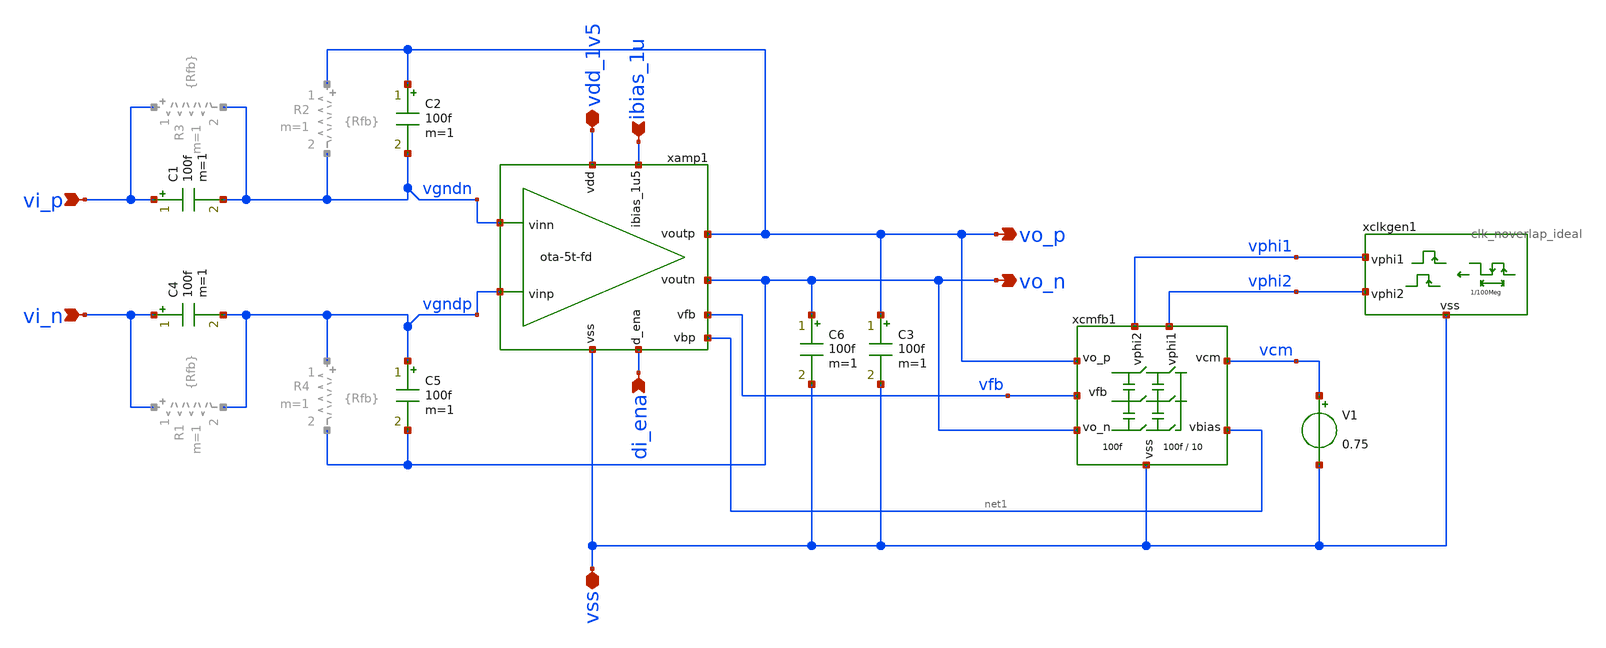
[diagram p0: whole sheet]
** sch_path: xschem/amp-cfb.sch
* xschem/ota-5t-fd.sch:
* (c) 2025 M. Koefinger
**.subckt amp-cfb vi_p vi_n di_ena vss vdd_1v5 ibias_1u vo_n vo_p
*.ipin vi_p
*.ipin vi_n
*.ipin di_ena
*.iopin vss
*.iopin vdd_1v5
*.ipin ibias_1u
*.opin vo_n
*.opin vo_p
C1 vi_p vgndn 100f m=1
C2 vo_p vgndn 100f m=1
C3 vo_p vss 100f m=1
C4 vi_n vgndp 100f m=1
C5 vgndp vo_n 100f m=1
C6 vo_n vss 100f m=1
xamp1 vdd_1v5 vfb vo_p vo_n vgndp vgndn ibias_1u di_ena vss net1 ota-5t-fd
xcmfb1 vphi1 vphi2 vss vo_p vcm net1 vfb vo_n cmfb_sc cap=100f div=10
xclkgen1 vphi1 vphi2 vss clk_noverlap_ideal fs=100Meg tnover=2n tdelay=0 trf=0.1n
V1 vcm vss 0.75
**.ends

* expanding   symbol:  ota-5t-fd.sym # of pins=10
** sym_path: xschem/ota-5t-fd.sym
** sch_path: xschem/ota-5t-fd.sch
.subckt ota-5t-fd vdd vfb voutp voutn vinp vinn ibias_1u5 d_ena vss vbp
*.ipin ibias_1u5
*.iopin vdd
*.iopin vss
*.ipin vinp
*.ipin vinn
*.opin voutn
*.ipin d_ena
*.opin voutp
*.ipin vfb
*.opin vbp
XMN3 tail gate_n vss vss sg13_lv_nmos w=2.5u l=0.5u ng=5 m=1 mm_ok=1
XMP2 voutp vfb vdd vdd sg13_lv_pmos w=0.5u l=0.5u ng=1 m=1 mm_ok=1
XMN1 voutn vinp tail vss sg13_lv_nmos w=5.5u l=0.5u ng=11 m=1 mm_ok=1
XMN2 voutp vinn tail vss sg13_lv_nmos w=5.5u l=0.5u ng=11 m=1 mm_ok=1
XMP1 voutn vfb vdd vdd sg13_lv_pmos w=0.5u l=0.5u ng=1 m=1 mm_ok=1
XMN4 ibias_1u5 gate_n vss vss sg13_lv_nmos w=1.5u l=0.5u ng=3 m=1 mm_ok=1
XMN5 gate_n ena_n vss vss sg13_lv_nmos w=0.5u l=0.13u ng=1 m=1 mm_ok=1
XMPSW1 vfb ena vdd vdd sg13_lv_pmos w=1.5u l=0.13u ng=1 m=1 mm_ok=1
XMN8 ena ena_n vss vss sg13_lv_nmos w=0.5u l=0.13u ng=1 m=1 mm_ok=1
XMP5 ena ena_n vdd vdd sg13_lv_pmos w=1.5u l=0.13u ng=1 m=1 mm_ok=1
XMN6 ibias_1u5 ena gate_n vss sg13_lv_nmos w=0.5u l=0.13u ng=1 m=1 mm_ok=1
XMN7 ena_n d_ena vss vss sg13_lv_nmos w=0.5u l=0.13u ng=1 m=1 mm_ok=1
XMP4 ena_n d_ena vdd vdd sg13_lv_pmos w=1.5u l=0.13u ng=1 m=1 mm_ok=1
XMN9 vbp gate_n vss vss sg13_lv_nmos w=1u l=0.5u ng=2 m=1 mm_ok=1
XMP3 vbp vbp vdd vdd sg13_lv_pmos w=0.5u l=0.5u ng=1 m=1 mm_ok=1
.ends


* expanding   symbol:  cmfb_sc.sym # of pins=8
** sym_path: xschem/cmfb_sc.sym
** sch_path: xschem/cmfb_sc.sch
.subckt cmfb_sc vphi2 vphi1 vss vo_p vcm vbias vfb vo_n  cap=100f div=10
*.ipin vcm
*.ipin vphi2
*.ipin vphi1
*.iopin vss
*.ipin vbias
*.iopin vo_p
*.iopin vo_n
*.opin vfb
C1 vo_p vfb 100f m=1
C2 net1 net2 10f m=1
C3 vfb vo_n 100f m=1
C4 net2 net3 10f m=1
S3 net1 vo_p vphi1 vss SW1
S4 vcm net1 vphi2 vss SW1
S6 net2 vfb vphi1 vss SW1
S7 vbias net2 vphi2 vss SW1
S9 net3 vo_n vphi1 vss SW1
S10 vcm net3 vphi2 vss SW1
.ends


* expanding   symbol:  clk_noverlap_ideal.sym # of pins=3
** sym_path: xschem/clk_noverlap_ideal.sym
** sch_path: xschem/clk_noverlap_ideal.sch
.subckt clk_noverlap_ideal vphi1 vphi2 vss  fs=100Meg tnover=2n tdelay=0 trf=0.1n
*.iopin vss
*.opin vphi1
*.opin vphi2
V1 vphi1 vss 0 PULSE 0 1.5 {tdelay} {trf} {trf} {0.5/{fs}-{tnover}} {1/{fs}} 0
V2 vphi2 vss 0 PULSE 0 1.5 {{tdelay}+{0.5/{fs}}} {trf} {trf} {0.5/{fs}-{tnover}} {1/{fs}} 0
.ends

**** begin user architecture code
.MODEL SW1 SW( VT=0.75 VH=0.01 RON=1 ROFF=1G )
**** end user architecture code
.end
